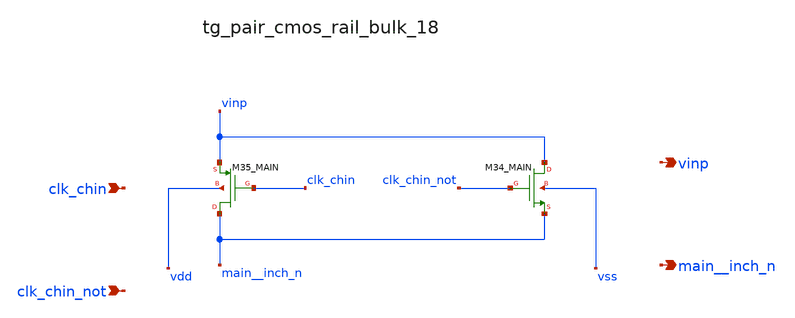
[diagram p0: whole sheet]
** sch_path: analog-db/raw/ia_004_fan_chopper_rrl/hier/blocks/tg_pair_cmos_rail_bulk_18.sch
**.subckt tg_pair_cmos_rail_bulk_18 clk_chin clk_chin_not vinp main__inch_n
*.ipin clk_chin
*.ipin clk_chin_not
*.opin vinp
*.opin main__inch_n
XM34_MAIN vinp clk_chin_not main__inch_n vss sg13_lv_nmos w=x_dut_xm34_main_w l=x_dut_xm34_main_l
+ ng=1 m=x_dut_xm34_main_m
XM35_MAIN main__inch_n clk_chin vinp vdd sg13_lv_pmos w=x_dut_xm35_main_w l=x_dut_xm35_main_l ng=1
+ m=x_dut_xm35_main_m
**.ends
.end
